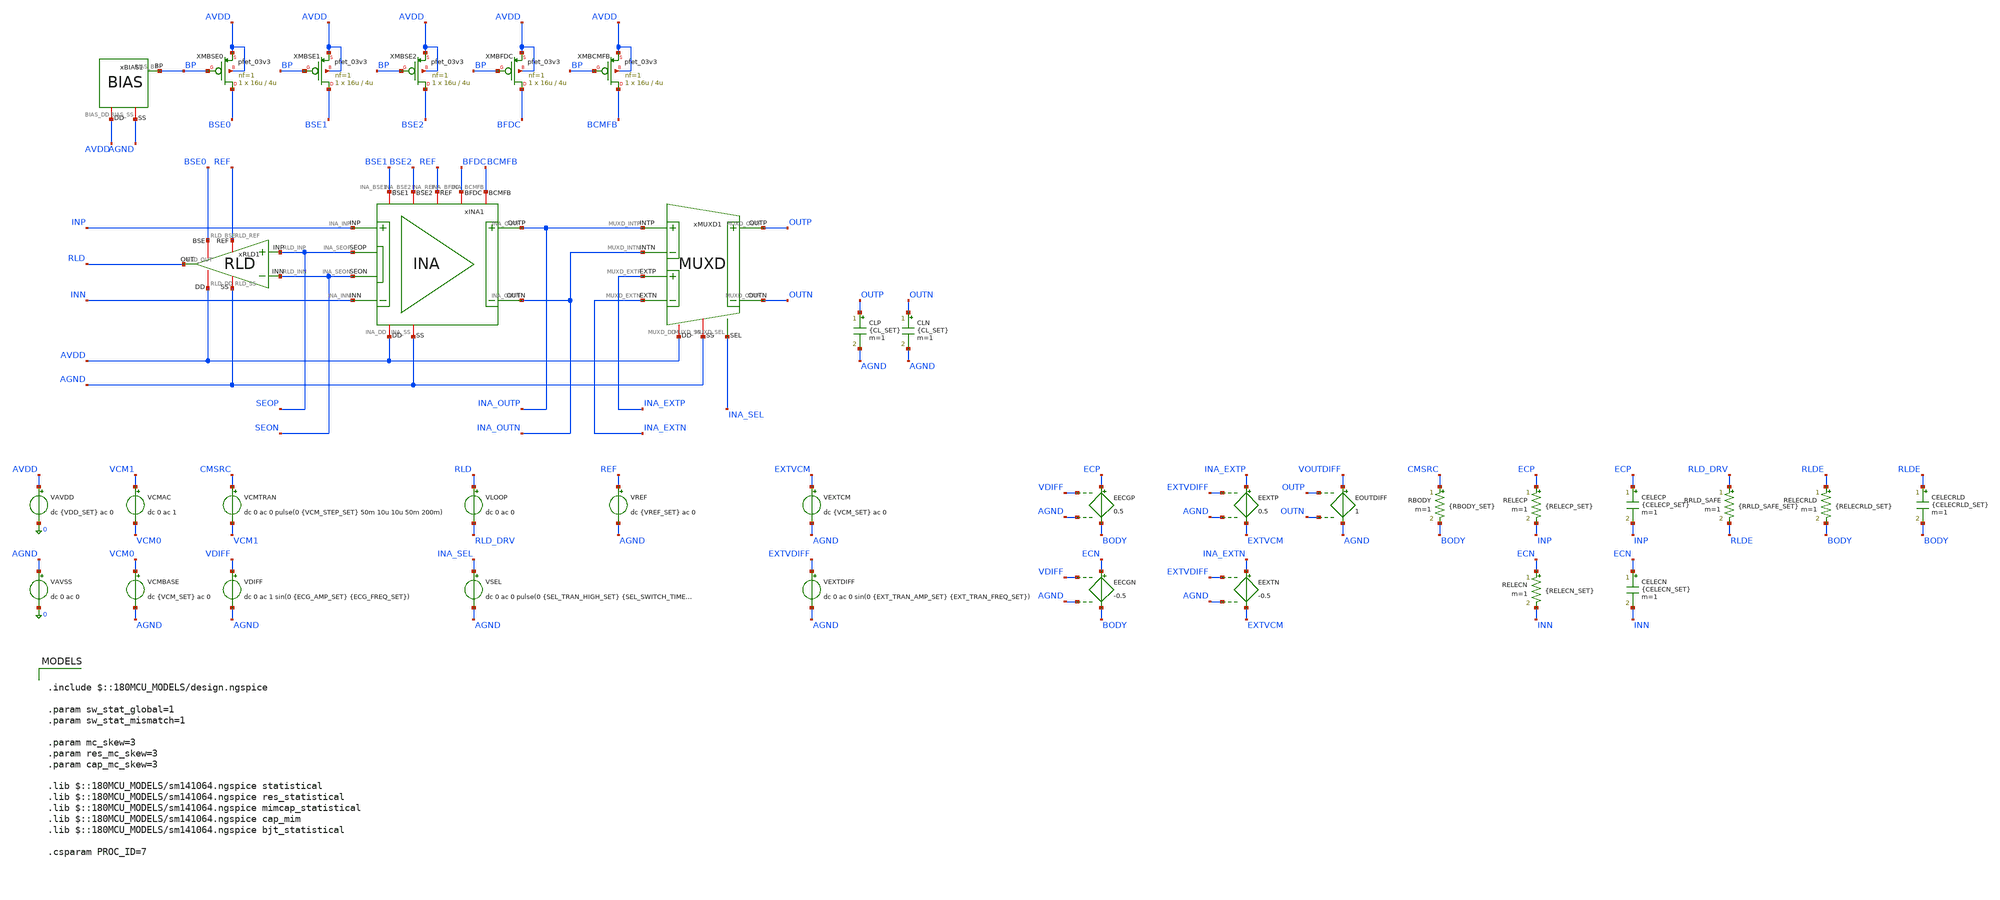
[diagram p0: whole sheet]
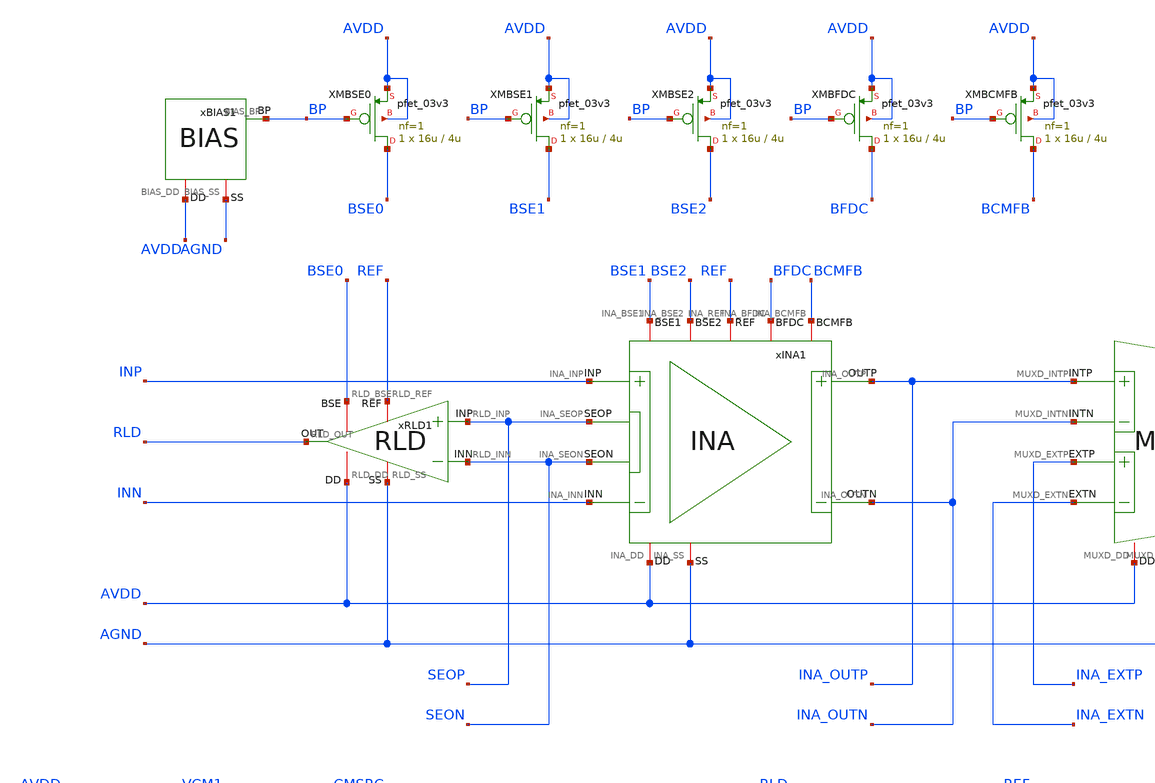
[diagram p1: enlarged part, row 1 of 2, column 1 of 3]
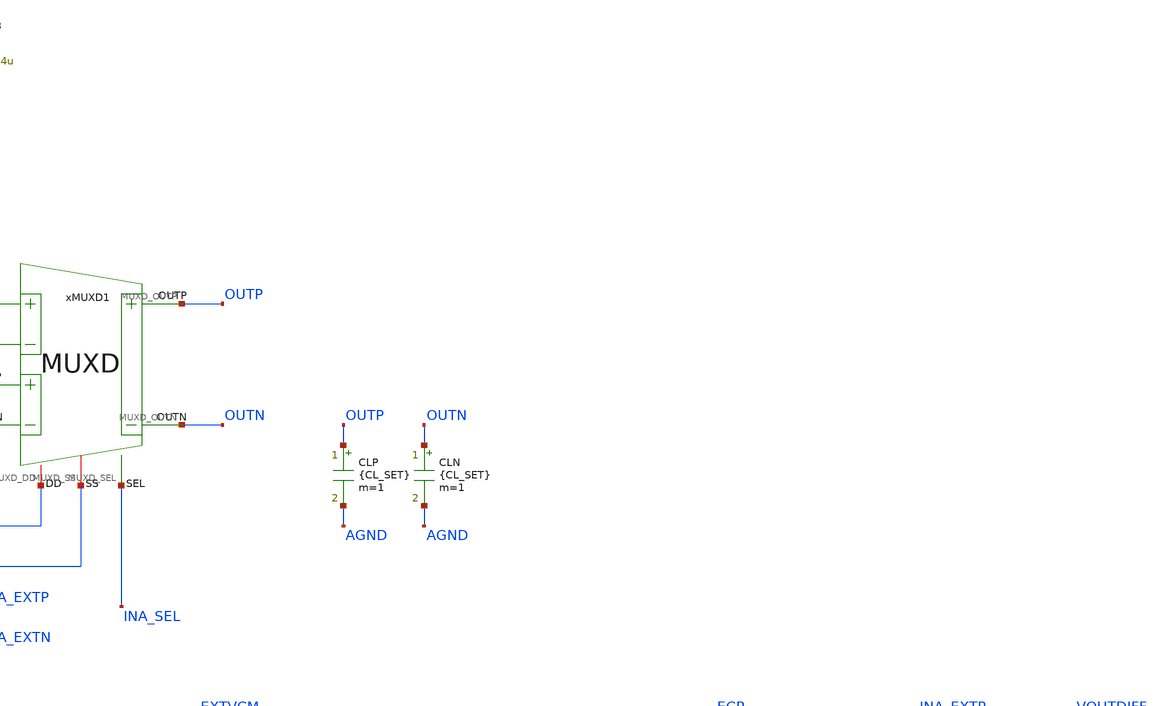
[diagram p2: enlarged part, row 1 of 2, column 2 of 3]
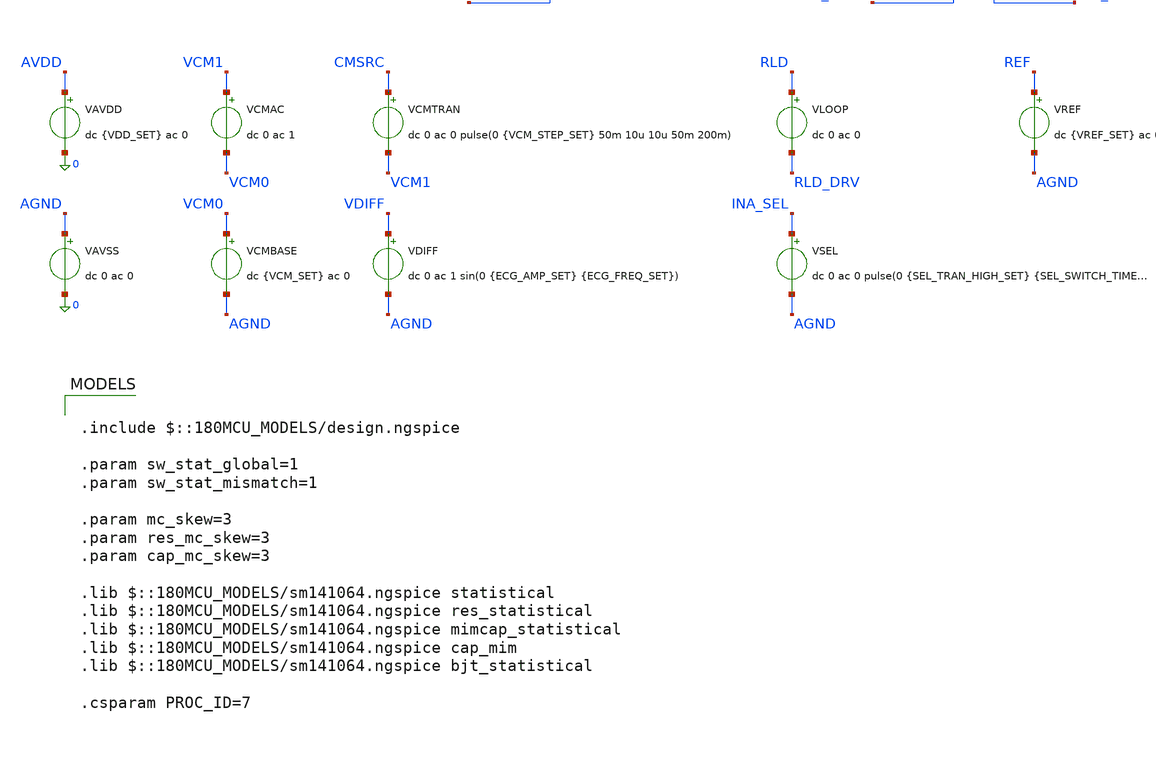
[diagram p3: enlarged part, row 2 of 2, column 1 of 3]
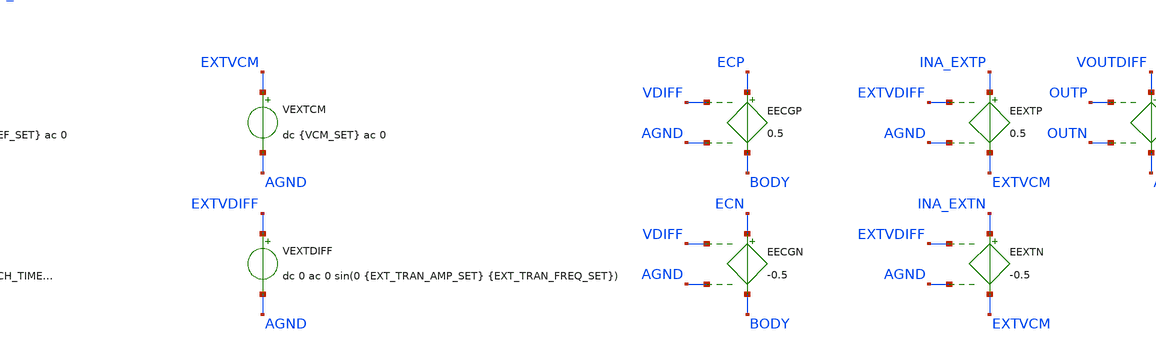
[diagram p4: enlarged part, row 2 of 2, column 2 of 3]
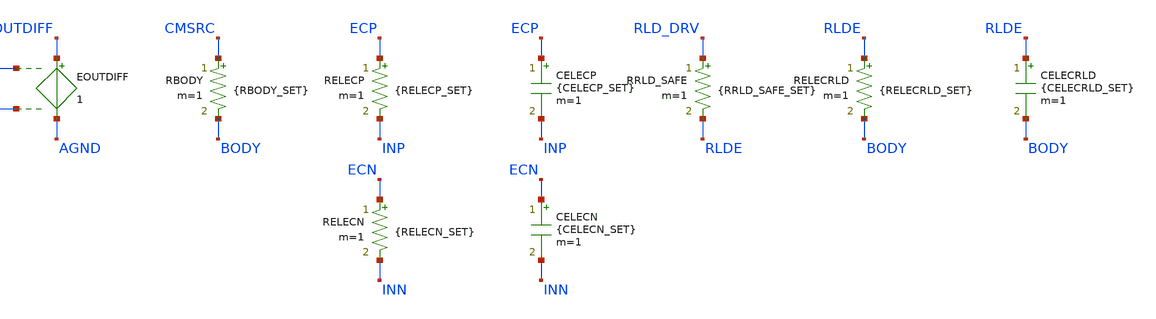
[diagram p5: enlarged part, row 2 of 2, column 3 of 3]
** sch_path: Design_Files/IC Design/Testbench/AFE_BLOCKS/INA_RLD/INA_RLD_TB_FULL.sch
**.subckt INA_RLD_TB_FULL
xINA1 AVDD AGND INP INN INA_OUTN BFDC INA_OUTP BCMFB REF SEON SEOP BSE1 BSE2 INA
xRLD1 AVDD AGND SEOP SEON RLD REF BSE0 RLD
CLP OUTP AGND {CL_SET} m=1
CLN OUTN AGND {CL_SET} m=1
xBIAS1 AVDD AGND BP BIAS
XMBSE0 BSE0 BP AVDD AVDD pfet_03v3 L=4u W=16u nf=1 ad='int((nf+1)/2) * W/nf * 0.18u' as='int((nf+2)/2) * W/nf * 0.18u'
+ pd='2*int((nf+1)/2) * (W/nf + 0.18u)' ps='2*int((nf+2)/2) * (W/nf + 0.18u)' nrd='0.18u / W' nrs='0.18u / W'
+ sa=0 sb=0 sd=0 m=1
XMBSE1 BSE1 BP AVDD AVDD pfet_03v3 L=4u W=16u nf=1 ad='int((nf+1)/2) * W/nf * 0.18u' as='int((nf+2)/2) * W/nf * 0.18u'
+ pd='2*int((nf+1)/2) * (W/nf + 0.18u)' ps='2*int((nf+2)/2) * (W/nf + 0.18u)' nrd='0.18u / W' nrs='0.18u / W'
+ sa=0 sb=0 sd=0 m=1
XMBSE2 BSE2 BP AVDD AVDD pfet_03v3 L=4u W=16u nf=1 ad='int((nf+1)/2) * W/nf * 0.18u' as='int((nf+2)/2) * W/nf * 0.18u'
+ pd='2*int((nf+1)/2) * (W/nf + 0.18u)' ps='2*int((nf+2)/2) * (W/nf + 0.18u)' nrd='0.18u / W' nrs='0.18u / W'
+ sa=0 sb=0 sd=0 m=1
XMBFDC BFDC BP AVDD AVDD pfet_03v3 L=4u W=16u nf=1 ad='int((nf+1)/2) * W/nf * 0.18u' as='int((nf+2)/2) * W/nf * 0.18u'
+ pd='2*int((nf+1)/2) * (W/nf + 0.18u)' ps='2*int((nf+2)/2) * (W/nf + 0.18u)' nrd='0.18u / W' nrs='0.18u / W'
+ sa=0 sb=0 sd=0 m=1
XMBCMFB BCMFB BP AVDD AVDD pfet_03v3 L=4u W=16u nf=1 ad='int((nf+1)/2) * W/nf * 0.18u' as='int((nf+2)/2) * W/nf * 0.18u'
+ pd='2*int((nf+1)/2) * (W/nf + 0.18u)' ps='2*int((nf+2)/2) * (W/nf + 0.18u)' nrd='0.18u / W' nrs='0.18u / W'
+ sa=0 sb=0 sd=0 m=1
VAVDD AVDD 0 dc {VDD_SET} ac 0
.save i(vavdd)
VCMBASE VCM0 AGND dc {VCM_SET} ac 0
VCMAC VCM1 VCM0 dc 0 ac 1
VAVSS AGND 0 dc 0 ac 0
VCMTRAN CMSRC VCM1 dc 0 ac 0 pulse(0 {VCM_STEP_SET} 50m 10u 10u 50m 200m)
EECGP ECP BODY VDIFF AGND 0.5
EECGN ECN BODY VDIFF AGND -0.5
EEXTP INA_EXTP EXTVCM EXTVDIFF AGND 0.5
VDIFF VDIFF AGND dc 0 ac 1 sin(0 {ECG_AMP_SET} {ECG_FREQ_SET})
VLOOP RLD RLD_DRV dc 0 ac 0
.save i(vloop)
VSEL INA_SEL AGND dc 0 ac 0 pulse(0 {SEL_TRAN_HIGH_SET} {SEL_SWITCH_TIME_SET} 1u 1u 400m 800m)
VEXTCM EXTVCM AGND dc {VCM_SET} ac 0
VEXTDIFF EXTVDIFF AGND dc 0 ac 0 sin(0 {EXT_TRAN_AMP_SET} {EXT_TRAN_FREQ_SET})
EEXTN INA_EXTN EXTVCM EXTVDIFF AGND -0.5
EOUTDIFF VOUTDIFF AGND OUTP OUTN 1
RBODY CMSRC BODY {RBODY_SET} m=1
RELECP ECP INP {RELECP_SET} m=1
RELECN ECN INN {RELECN_SET} m=1
CELECP ECP INP {CELECP_SET} m=1
CELECN ECN INN {CELECN_SET} m=1
RRLD_SAFE RLD_DRV RLDE {RRLD_SAFE_SET} m=1
RELECRLD RLDE BODY {RELECRLD_SET} m=1
CELECRLD RLDE BODY {CELECRLD_SET} m=1
VREF REF AGND dc {VREF_SET} ac 0
.save i(vref)
xMUXD1 AVDD AGND INA_OUTP INA_OUTN OUTN OUTP INA_EXTP INA_EXTN INA_SEL MUXD
**** begin user architecture code

.include $::180MCU_MODELS/design.ngspice

.param sw_stat_global=1
.param sw_stat_mismatch=1

.param mc_skew=3
.param res_mc_skew=3
.param cap_mc_skew=3

.lib $::180MCU_MODELS/sm141064.ngspice statistical
.lib $::180MCU_MODELS/sm141064.ngspice res_statistical
.lib $::180MCU_MODELS/sm141064.ngspice mimcap_statistical
.lib $::180MCU_MODELS/sm141064.ngspice cap_mim
.lib $::180MCU_MODELS/sm141064.ngspice bjt_statistical

.csparam PROC_ID=7



.param VDD_SET=3.3
.param TEMP_SET=27
.param VCM_SET={VDD_SET/2}
.param VREF_SET={VDD_SET/2}

.param CL_SET=10p

.param ECG_AMP_SET=0.5m
.param ECG_FREQ_SET=10
.param VCM_STEP_SET=300m

.param RBODY_SET=100Meg

.param RELECP_SET=100k
.param RELECN_SET=100k
.param CELECP_SET=100n
.param CELECN_SET=100n

.param RRLD_SAFE_SET=1Meg
.param RELECRLD_SET=100k
.param CELECRLD_SET=100n

.param SEL_TRAN_HIGH_SET=0
.param SEL_SWITCH_TIME_SET=200m
.param EXT_TRAN_AMP_SET=0
.param EXT_TRAN_FREQ_SET=25

.csparam MC_RUNS=200

.temp {TEMP_SET}

.options gmin=1e-12
.options rshunt=1e12
.options method=gear





.control

destroy all

set noaskquit
set wr_singlescale
unset wr_vecnames

option klu
option numdgt=15
option method=gear
option maxord=2
option plotwinsize=0
option rshunt=1e12


if $&PROC_ID = 5
set proc=MM
else
if $&PROC_ID = 6
set proc=GL
else
set proc=FULL
end
end


shell mkdir -p /foss/designs/ECG_Acquisition_IC/Measurement_Results/IC_Simulation/AFE_BLOCKS/INA_RLD/{$proc}.Result_txt

shell rm -f /foss/designs/ECG_Acquisition_IC/Measurement_Results/IC_Simulation/AFE_BLOCKS/INA_RLD/{$proc}.Result_txt/{$proc}.mc_summary.txt
shell rm -f /foss/designs/ECG_Acquisition_IC/Measurement_Results/IC_Simulation/AFE_BLOCKS/INA_RLD/{$proc}.Result_txt/{$proc}.mc_debug_op.txt


echo run idd_A power_W out_cm_error_V rld_dc_error_V vos_V s1_gain s2_gain ina_gain gain_error_pct rld_ugf_Hz
+ rld_pm_deg cm_supp_60_dB cm_supp_150_dB ina_cmrr_60_dB ina_cmrr_150_dB > /foss/designs/ECG_Acquisition_IC/Measurement_Results/IC_Simulation/AFE_BLOCKS/INA_RLD/{$proc}.Result_txt/{$proc}.mc_summary.txt

echo run vos_V outp_V outn_V outcm_V outdiff_V ref_V rld_V body_V bp_V idd_A power_W > /foss/designs/ECG_Acquisition_IC/Measurement_Results/IC_Simulation/AFE_BLOCKS/INA_RLD/{$proc}.Result_txt/{$proc}.mc_debug_op.txt


let run=1
let mc_runs=$&MC_RUNS


dowhile run <= mc_runs

set runnum=$&run

setseed $runnum
mc_source


option klu
option numdgt=15
option method=gear
option maxord=2
option plotwinsize=0
option rshunt=1e12


* SOURCES

alter @VAVDD[DC]=3.3
alter @VAVSS[DC]=0

alter @VCMBASE[DC]=1.65
alter @VCMAC[DC]=0
alter @VCMTRAN[DC]=0

alter @VDIFF[DC]=0
alter @VLOOP[DC]=0

alter @VSEL[DC]=0

alter @VEXTCM[DC]=1.65
alter @VEXTDIFF[DC]=0

alter @VREF[DC]=1.65

alter @VAVDD[ACMAG]=0
alter @VAVSS[ACMAG]=0
alter @VCMBASE[ACMAG]=0
alter @VCMAC[ACMAG]=0
alter @VCMTRAN[ACMAG]=0
alter @VDIFF[ACMAG]=0
alter @VLOOP[ACMAG]=0
alter @VEXTCM[ACMAG]=0
alter @VEXTDIFF[ACMAG]=0
alter @VREF[ACMAG]=0


* BAL

alter RELECP 100k
alter RELECN 100k
alter CELECP 100n
alter CELECN 100n

alter RRLD_SAFE 1Meg


save AVDD AGND BP REF
save INP INN SEOP SEON
save INA_OUTP INA_OUTN
save OUTP OUTN
save RLD RLD_DRV BODY CMSRC
save VDIFF

save vavdd#branch
save vloop#branch

save @m.xmbse0.m0[id]
save @m.xmbse1.m0[id]
save @m.xmbse2.m0[id]
save @m.xmbfdc.m0[id]
save @m.xmbcmfb.m0[id]


* OFFSET

alter @VDIFF[DC]=0

dc VDIFF -10m 10m 10u

let outdiff_sweep=v(INA_OUTP)-v(INA_OUTN)

meas dc vos_meas when outdiff_sweep=0 cross=1

set vos_val=$&vos_meas

destroy all


* CENTER OP

alter @VDIFF[DC]=$vos_val

alter @VDIFF[ACMAG]=0
alter @VCMAC[ACMAG]=0
alter @VLOOP[ACMAG]=0
alter @VAVDD[ACMAG]=0
alter @VAVSS[ACMAG]=0
alter @VREF[ACMAG]=0

alter RRLD_SAFE 1Meg

op

let outp=v(OUTP)-v(AGND)
let outn=v(OUTN)-v(AGND)

let outcm=0.5*(outp+outn)
let outdiff=outp-outn

let ref=v(REF)-v(AGND)

let rld=v(RLD)-v(AGND)
let body=v(BODY)-v(AGND)
let bp=v(BP)-v(AGND)

let out_cm_error=outcm-ref
let rld_dc_error=rld-ref

let idd_total=abs(vavdd#branch)
let power_total=(v(AVDD)-v(AGND))*idd_total

set outp_val=$&outp
set outn_val=$&outn
set outcm_val=$&outcm
set outdiff_val=$&outdiff

set ref_val=$&ref
set rld_val=$&rld
set body_val=$&body
set bp_val=$&bp

set out_cm_error_val=$&out_cm_error
set rld_dc_error_val=$&rld_dc_error

set idd_val=$&idd_total
set power_val=$&power_total


echo $runnum $vos_val $outp_val $outn_val $outcm_val $outdiff_val $ref_val $rld_val $body_val $bp_val
+ $idd_val $power_val >> /foss/designs/ECG_Acquisition_IC/Measurement_Results/IC_Simulation/AFE_BLOCKS/INA_RLD/{$proc}.Result_txt/{$proc}.mc_debug_op.txt

destroy all


* INA AC

alter RRLD_SAFE 1Meg

alter @VDIFF[DC]=$vos_val

alter @VDIFF[ACMAG]=1
alter @VDIFF[ACPHASE]=0

alter @VCMAC[ACMAG]=0
alter @VLOOP[ACMAG]=0
alter @VEXTDIFF[ACMAG]=0
alter @VAVDD[ACMAG]=0
alter @VAVSS[ACMAG]=0
alter @VREF[ACMAG]=0

ac dec 100 0.01 10Meg

let vin_diff=v(INP)-v(INN)
let se_diff=v(SEOP)-v(SEON)
let ina_out_diff=v(INA_OUTP)-v(INA_OUTN)

let s1_gain=mag(se_diff/vin_diff)
let s2_gain=mag(ina_out_diff/se_diff)
let ina_gain=mag(ina_out_diff/vin_diff)

meas ac s1_gain_10_meas find s1_gain at=10
meas ac s2_gain_10_meas find s2_gain at=10
meas ac ina_gain_10_meas find ina_gain at=10

meas ac ina_gain_60_meas find ina_gain at=60
meas ac ina_gain_150_meas find ina_gain at=150

let gain_error_pct=100*(ina_gain_10_meas/240-1)

set s1_gain_val=$&s1_gain_10_meas
set s2_gain_val=$&s2_gain_10_meas
set ina_gain_val=$&ina_gain_10_meas

set ina_gain_60_val=$&ina_gain_60_meas
set ina_gain_150_val=$&ina_gain_150_meas

set gain_error_val=$&gain_error_pct

destroy all


* RLD OFF + INA CMRR

alter RRLD_SAFE 1e15

alter @VDIFF[ACMAG]=0

alter @VCMAC[ACMAG]=1
alter @VCMAC[ACPHASE]=0

alter @VLOOP[ACMAG]=0
alter @VEXTDIFF[ACMAG]=0
alter @VAVDD[ACMAG]=0
alter @VAVSS[ACMAG]=0
alter @VREF[ACMAG]=0

ac dec 100 0.01 10Meg

let vin_cm=0.5*(v(INP)+v(INN))-v(AGND)
let ina_out_diff=v(INA_OUTP)-v(INA_OUTN)

let vin_cm_mag=mag(vin_cm)
let ina_acm=mag(ina_out_diff/vin_cm)

meas ac vin_cm_off_60_meas find vin_cm_mag at=60
meas ac vin_cm_off_150_meas find vin_cm_mag at=150

meas ac ina_acm_60_meas find ina_acm at=60
meas ac ina_acm_150_meas find ina_acm at=150

set vin_cm_off_60_val=$&vin_cm_off_60_meas
set vin_cm_off_150_val=$&vin_cm_off_150_meas

set ina_acm_60_val=$&ina_acm_60_meas
set ina_acm_150_val=$&ina_acm_150_meas

let ina_cmrr_60=20*log10($ina_gain_60_val/$ina_acm_60_val)
let ina_cmrr_150=20*log10($ina_gain_150_val/$ina_acm_150_val)

set ina_cmrr_60_val=$&ina_cmrr_60
set ina_cmrr_150_val=$&ina_cmrr_150

destroy all


* RLD ON

alter RRLD_SAFE 1Meg

alter @VDIFF[ACMAG]=0

alter @VCMAC[ACMAG]=1
alter @VCMAC[ACPHASE]=0

alter @VLOOP[ACMAG]=0
alter @VEXTDIFF[ACMAG]=0
alter @VAVDD[ACMAG]=0
alter @VAVSS[ACMAG]=0
alter @VREF[ACMAG]=0

ac dec 100 0.01 10Meg

let vin_cm=0.5*(v(INP)+v(INN))-v(AGND)
let vin_cm_mag=mag(vin_cm)

meas ac vin_cm_on_60_meas find vin_cm_mag at=60
meas ac vin_cm_on_150_meas find vin_cm_mag at=150

set vin_cm_on_60_val=$&vin_cm_on_60_meas
set vin_cm_on_150_val=$&vin_cm_on_150_meas

let cm_supp_60=20*log10($vin_cm_off_60_val/$vin_cm_on_60_val)
let cm_supp_150=20*log10($vin_cm_off_150_val/$vin_cm_on_150_val)

set cm_supp_60_val=$&cm_supp_60
set cm_supp_150_val=$&cm_supp_150

destroy all


* RLD LOOP

alter RRLD_SAFE 1Meg

alter @VDIFF[ACMAG]=0
alter @VCMAC[ACMAG]=0

alter @VLOOP[ACMAG]=1
alter @VLOOP[ACPHASE]=0

alter @VEXTDIFF[ACMAG]=0
alter @VAVDD[ACMAG]=0
alter @VAVSS[ACMAG]=0
alter @VREF[ACMAG]=0

ac dec 100 0.01 10Meg

let loop_in=v(RLD_DRV)-v(AGND)
let loop_out=v(RLD)-v(AGND)

let loop_tf=-loop_out/loop_in

let loop_gain=mag(loop_tf)
let loop_phase=(180/3.141592653589793)*cph(loop_tf)

meas ac rld_ugf_meas when loop_gain=1 fall=1

meas ac rld_phase_ugf_meas find loop_phase at=$&rld_ugf_meas

let rld_pm=180+rld_phase_ugf_meas

set rld_ugf_val=$&rld_ugf_meas
set rld_pm_val=$&rld_pm

destroy all


* SUMMARY

echo $runnum $idd_val $power_val $out_cm_error_val $rld_dc_error_val $vos_val $s1_gain_val $s2_gain_val
+ $ina_gain_val $gain_error_val $rld_ugf_val $rld_pm_val $cm_supp_60_val $cm_supp_150_val $ina_cmrr_60_val
+ $ina_cmrr_150_val >> /foss/designs/ECG_Acquisition_IC/Measurement_Results/IC_Simulation/AFE_BLOCKS/INA_RLD/{$proc}.Result_txt/{$proc}.mc_summary.txt


let run=run+1

end


quit

.endc


**** end user architecture code
**.ends
.end
